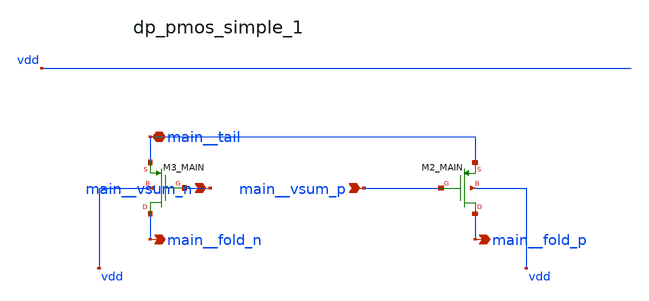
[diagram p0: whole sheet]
** sch_path: analog-db/raw/ia_004_fan_chopper_rrl/hier/blocks/dp_pmos_simple_1.sch
**.subckt dp_pmos_simple_1 main__vsum_n main__vsum_p main__tail main__fold_n main__fold_p
*.ipin main__vsum_n
*.ipin main__vsum_p
*.iopin main__tail
*.opin main__fold_n
*.opin main__fold_p
XM2_MAIN main__fold_p main__vsum_p main__tail vdd sg13_lv_pmos w=x_dut_xm2_main_w l=x_dut_xm2_main_l
+ ng=1 m=x_dut_xm2_main_m
XM3_MAIN main__fold_n main__vsum_n main__tail vdd sg13_lv_pmos w=x_dut_xm3_main_w l=x_dut_xm3_main_l
+ ng=1 m=x_dut_xm3_main_m
**.ends
.end
